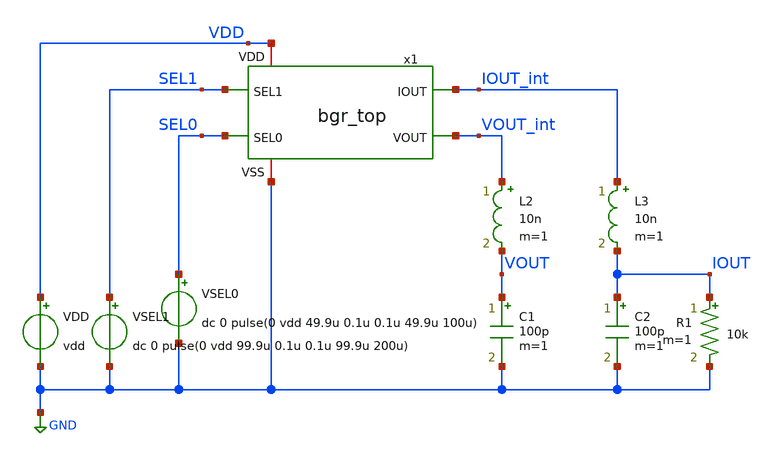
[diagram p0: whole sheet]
** sch_path: member_project/BGR/Maehashi/design/tb_bgr_top.sch
**.subckt tb_bgr_top
VDD VDD GND vdd
VSEL1 SEL1 GND dc 0 pulse(0 vdd 99.9u 0.1u 0.1u 99.9u 200u)
C1 VOUT GND 100p m=1
L2 VOUT_int VOUT 10n m=1
x1 SEL0 VDD IOUT_int VOUT_int GND SEL1 bgr_top
R1 IOUT GND 10k m=1
VSEL0 SEL0 GND dc 0 pulse(0 vdd 49.9u 0.1u 0.1u 49.9u 100u)
L3 IOUT_int IOUT 10n m=1
C2 IOUT GND 100p m=1
**** begin user architecture code


.option savecurrents
.temp 40
.param vdd = 5
.control
set units=degree
save all

alterparam vthMN = 0 ; Slow:0.1, Fast:-0.1
alterparam vthMP = 0 ; Slow:-0.1, Fast:0.1
alterparam magRS = 1 ; Slow:1.2, Fast:0.85
reset

tran 10n 200u
plot v(SEL1) v(SEL0)
*plot v(x1.x5.sel0i) v(x1.x5.sel1i) v(x1.x5.in0sel) v(x1.x5.in1sel) v(x1.x5.in2sel)
plot v(VOUT) v(x1.bgr_a_out) v(x1.bgr_b_out)
plot v(IOUT)
.endc

 .include $::LIB/ip62_models
**** end user architecture code
**.ends
.GLOBAL GND
.end
